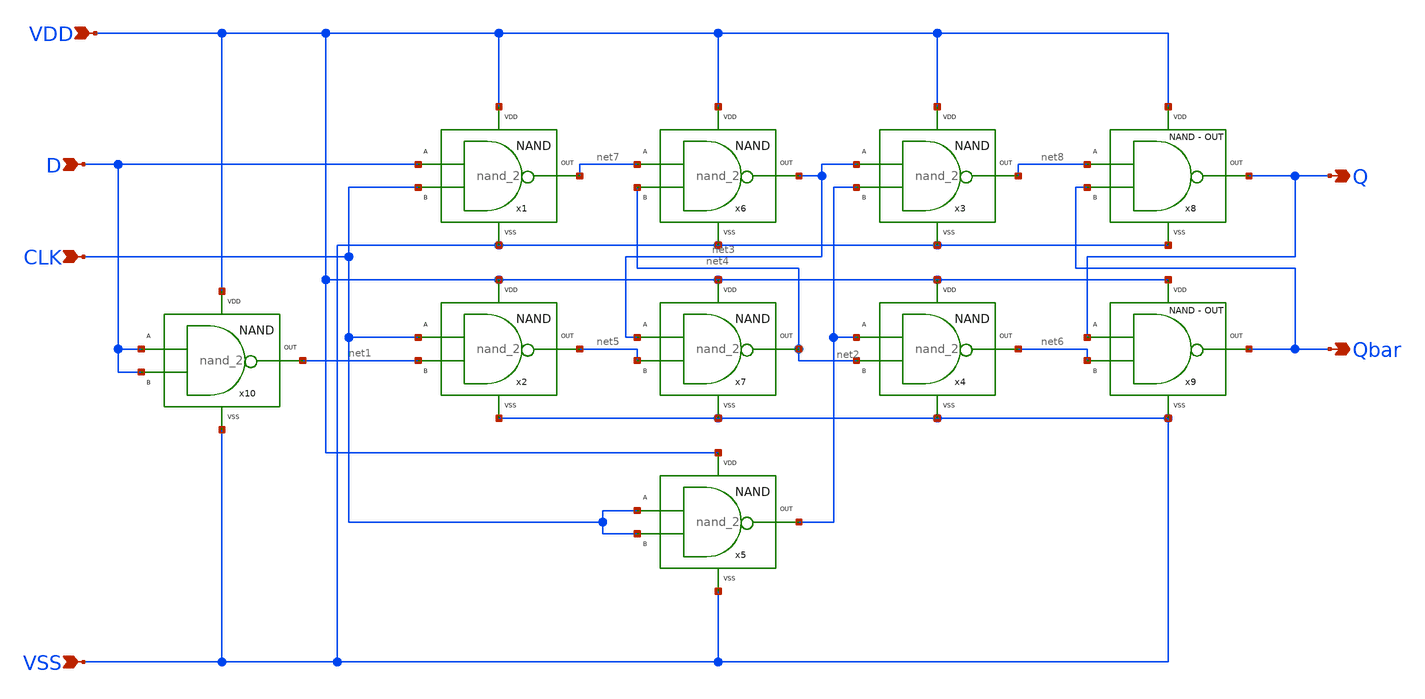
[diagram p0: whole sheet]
** sch_path: Project/1-on-chip/schematic/PNgen/dff_async2.sch
**.subckt dff_async2 VDD Q Qbar VSS CLK D
*.ipin VDD
*.opin Q
*.opin Qbar
*.ipin VSS
*.ipin CLK
*.ipin D
x1 D CLK VDD VSS net7 nand_2
x2 CLK net1 VDD VSS net5 nand_2
x3 net3 net2 VDD VSS net8 nand_2
x4 net2 net4 VDD VSS net6 nand_2
x5 CLK CLK VDD VSS net2 nand_2
x10 D D VDD VSS net1 nand_2
x6 net7 net4 VDD VSS net3 nand_2
x7 net3 net5 VDD VSS net4 nand_2
x8 net8 Qbar VDD VSS Q nand_2_out
x9 Q net6 VDD VSS Qbar nand_2_out
**.ends

* expanding   symbol:  nand_2.sym # of pins=5
** sym_path: Project/1-on-chip/schematic/PNgen/nand_2.sym
** sch_path: Project/1-on-chip/schematic/PNgen/nand_2.sch
.subckt nand_2 A B VDD VSS OUT
*.ipin VDD
*.opin OUT
*.ipin A
*.ipin B
*.ipin VSS
XM1 OUT A net1 VSS nfet_03v3 L=0.28u W=1.2u nf=1 ad='int((nf+1)/2) * W/nf * 0.18u' as='int((nf+2)/2) * W/nf * 0.18u'
+ pd='2*int((nf+1)/2) * (W/nf + 0.18u)' ps='2*int((nf+2)/2) * (W/nf + 0.18u)' nrd='0.18u / W' nrs='0.18u / W'
+ sa=0 sb=0 sd=0 m=1
XM2 OUT A VDD VDD pfet_03v3 L=0.28u W=1.3u nf=1 ad='int((nf+1)/2) * W/nf * 0.18u' as='int((nf+2)/2) * W/nf * 0.18u'
+ pd='2*int((nf+1)/2) * (W/nf + 0.18u)' ps='2*int((nf+2)/2) * (W/nf + 0.18u)' nrd='0.18u / W' nrs='0.18u / W'
+ sa=0 sb=0 sd=0 m=1
XM3 OUT B VDD VDD pfet_03v3 L=0.28u W=1.3u nf=1 ad='int((nf+1)/2) * W/nf * 0.18u' as='int((nf+2)/2) * W/nf * 0.18u'
+ pd='2*int((nf+1)/2) * (W/nf + 0.18u)' ps='2*int((nf+2)/2) * (W/nf + 0.18u)' nrd='0.18u / W' nrs='0.18u / W'
+ sa=0 sb=0 sd=0 m=1
XM4 net1 B VSS VSS nfet_03v3 L=0.28u W=1.2u nf=1 ad='int((nf+1)/2) * W/nf * 0.18u' as='int((nf+2)/2) * W/nf * 0.18u'
+ pd='2*int((nf+1)/2) * (W/nf + 0.18u)' ps='2*int((nf+2)/2) * (W/nf + 0.18u)' nrd='0.18u / W' nrs='0.18u / W'
+ sa=0 sb=0 sd=0 m=1
.ends


* expanding   symbol:  nand_2_out.sym # of pins=5
** sym_path: Project/1-on-chip/schematic/PNgen/nand_2_out.sym
** sch_path: Project/1-on-chip/schematic/PNgen/nand_2_out.sch
.subckt nand_2_out A B VDD VSS OUT
*.ipin VDD
*.opin OUT
*.ipin A
*.ipin B
*.ipin VSS
XM1 OUT A net1 VSS nfet_03v3 L=0.28u W=2.4u nf=1 ad='int((nf+1)/2) * W/nf * 0.18u' as='int((nf+2)/2) * W/nf * 0.18u'
+ pd='2*int((nf+1)/2) * (W/nf + 0.18u)' ps='2*int((nf+2)/2) * (W/nf + 0.18u)' nrd='0.18u / W' nrs='0.18u / W'
+ sa=0 sb=0 sd=0 m=1
XM2 OUT A VDD VDD pfet_03v3 L=0.28u W=2.6u nf=1 ad='int((nf+1)/2) * W/nf * 0.18u' as='int((nf+2)/2) * W/nf * 0.18u'
+ pd='2*int((nf+1)/2) * (W/nf + 0.18u)' ps='2*int((nf+2)/2) * (W/nf + 0.18u)' nrd='0.18u / W' nrs='0.18u / W'
+ sa=0 sb=0 sd=0 m=1
XM3 OUT B VDD VDD pfet_03v3 L=0.28u W=2.6u nf=1 ad='int((nf+1)/2) * W/nf * 0.18u' as='int((nf+2)/2) * W/nf * 0.18u'
+ pd='2*int((nf+1)/2) * (W/nf + 0.18u)' ps='2*int((nf+2)/2) * (W/nf + 0.18u)' nrd='0.18u / W' nrs='0.18u / W'
+ sa=0 sb=0 sd=0 m=1
XM4 net1 B VSS VSS nfet_03v3 L=0.28u W=2.4u nf=1 ad='int((nf+1)/2) * W/nf * 0.18u' as='int((nf+2)/2) * W/nf * 0.18u'
+ pd='2*int((nf+1)/2) * (W/nf + 0.18u)' ps='2*int((nf+2)/2) * (W/nf + 0.18u)' nrd='0.18u / W' nrs='0.18u / W'
+ sa=0 sb=0 sd=0 m=1
.ends

.end
